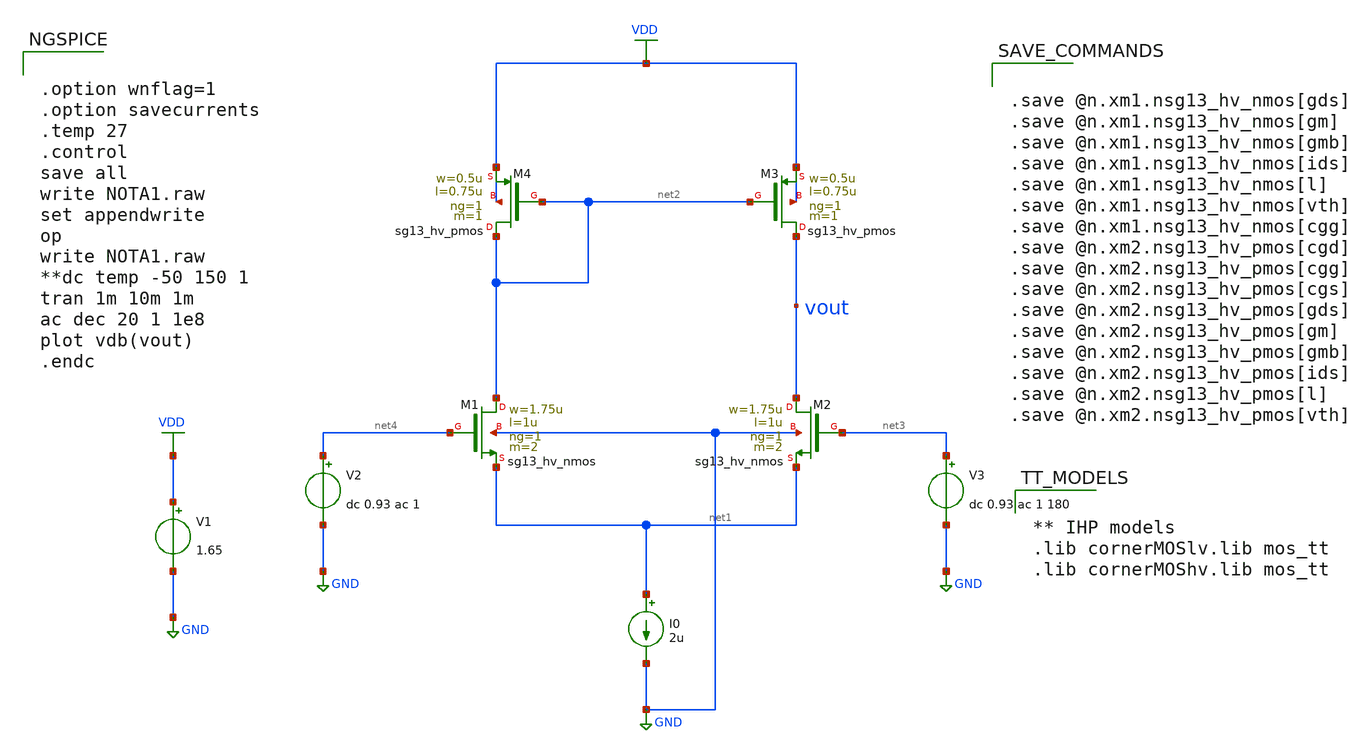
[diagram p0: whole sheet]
** sch_path: Design Files/RAMP/OTA/NOTA1.sch
**.subckt NOTA1
XM1 net2 net4 net1 GND sg13_hv_nmos w=1.75u l=1u ng=1 m=2 mm_ok=1
XM2 vout net3 net1 GND sg13_hv_nmos w=1.75u l=1u ng=1 m=2 mm_ok=1
I0 net1 GND 2u
XM3 vout net2 VDD VDD sg13_hv_pmos w=0.5u l=0.75u ng=1 m=1 mm_ok=1
XM4 net2 net2 VDD VDD sg13_hv_pmos w=0.5u l=0.75u ng=1 m=1 mm_ok=1
V1 VDD GND 1.65
V2 net4 GND dc 0.93 ac 1
V3 net3 GND dc 0.93 ac 1 180
**** begin user architecture code


.save @n.xm1.nsg13_hv_nmos[gds]
.save @n.xm1.nsg13_hv_nmos[gm]
.save @n.xm1.nsg13_hv_nmos[gmb]
.save @n.xm1.nsg13_hv_nmos[ids]
.save @n.xm1.nsg13_hv_nmos[l]
.save @n.xm1.nsg13_hv_nmos[vth]
.save @n.xm1.nsg13_hv_nmos[cgg]
.save @n.xm2.nsg13_hv_pmos[cgd]
.save @n.xm2.nsg13_hv_pmos[cgg]
.save @n.xm2.nsg13_hv_pmos[cgs]
.save @n.xm2.nsg13_hv_pmos[gds]
.save @n.xm2.nsg13_hv_pmos[gm]
.save @n.xm2.nsg13_hv_pmos[gmb]
.save @n.xm2.nsg13_hv_pmos[ids]
.save @n.xm2.nsg13_hv_pmos[l]
.save @n.xm2.nsg13_hv_pmos[vth]




.option wnflag=1
.option savecurrents
.temp 27
.control
save all
write NOTA1.raw
set appendwrite
op
write NOTA1.raw
**dc temp -50 150 1
tran 1m 10m 1m
ac dec 20 1 1e8
plot vdb(vout)
.endc




** IHP models
.lib cornerMOSlv.lib mos_tt
.lib cornerMOShv.lib mos_tt


**** end user architecture code
**.ends
.GLOBAL GND
.GLOBAL VDD
.end
